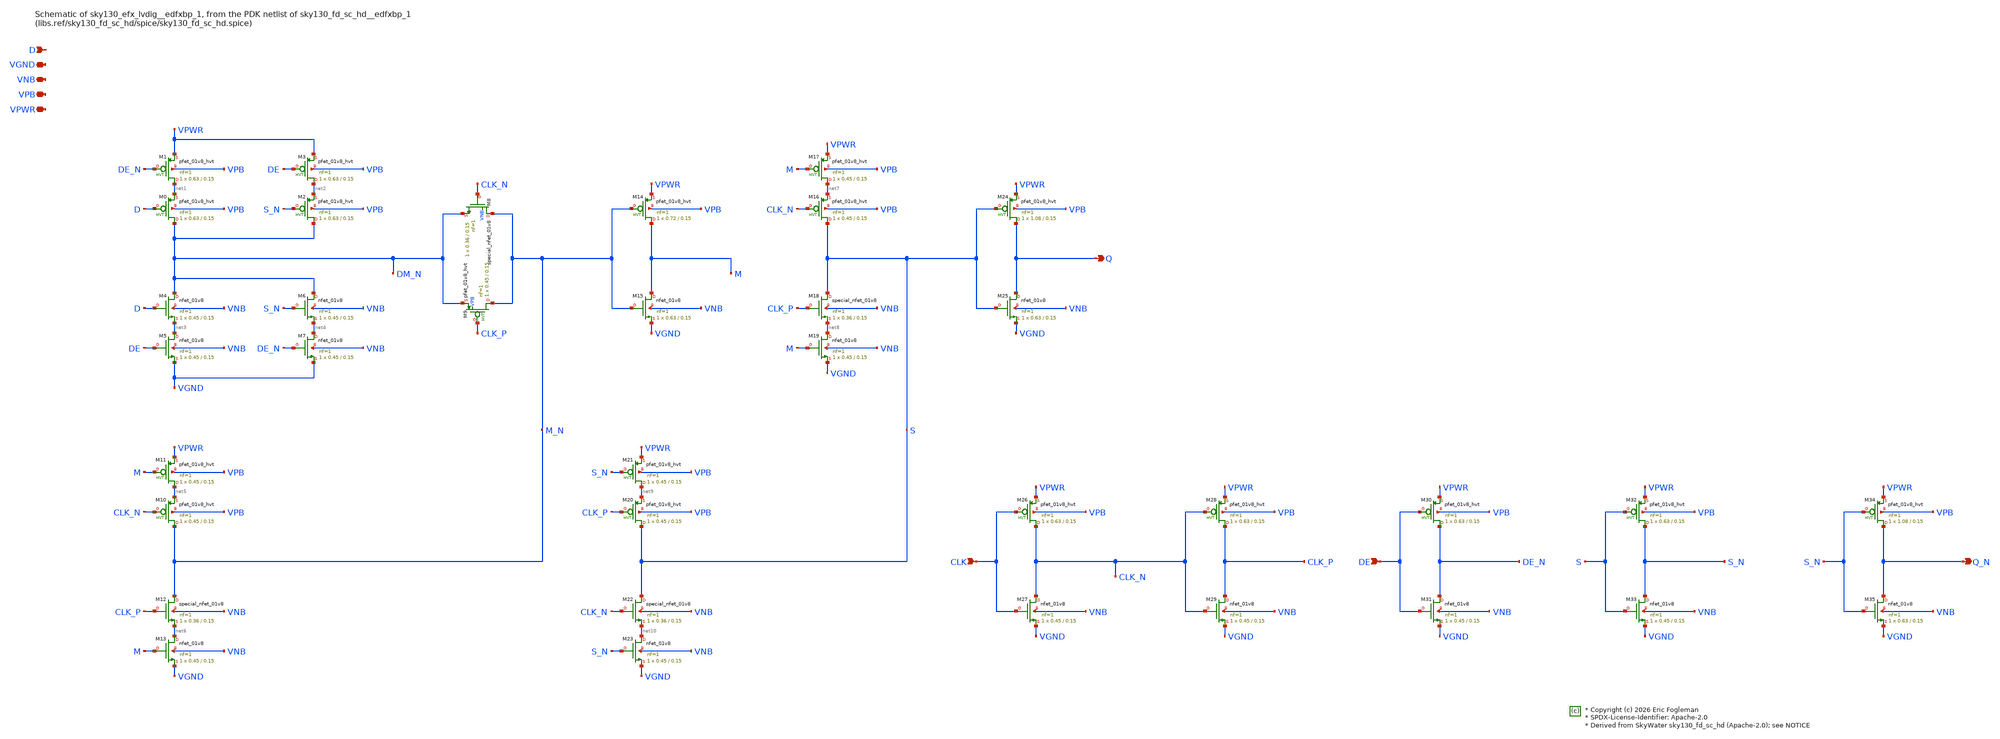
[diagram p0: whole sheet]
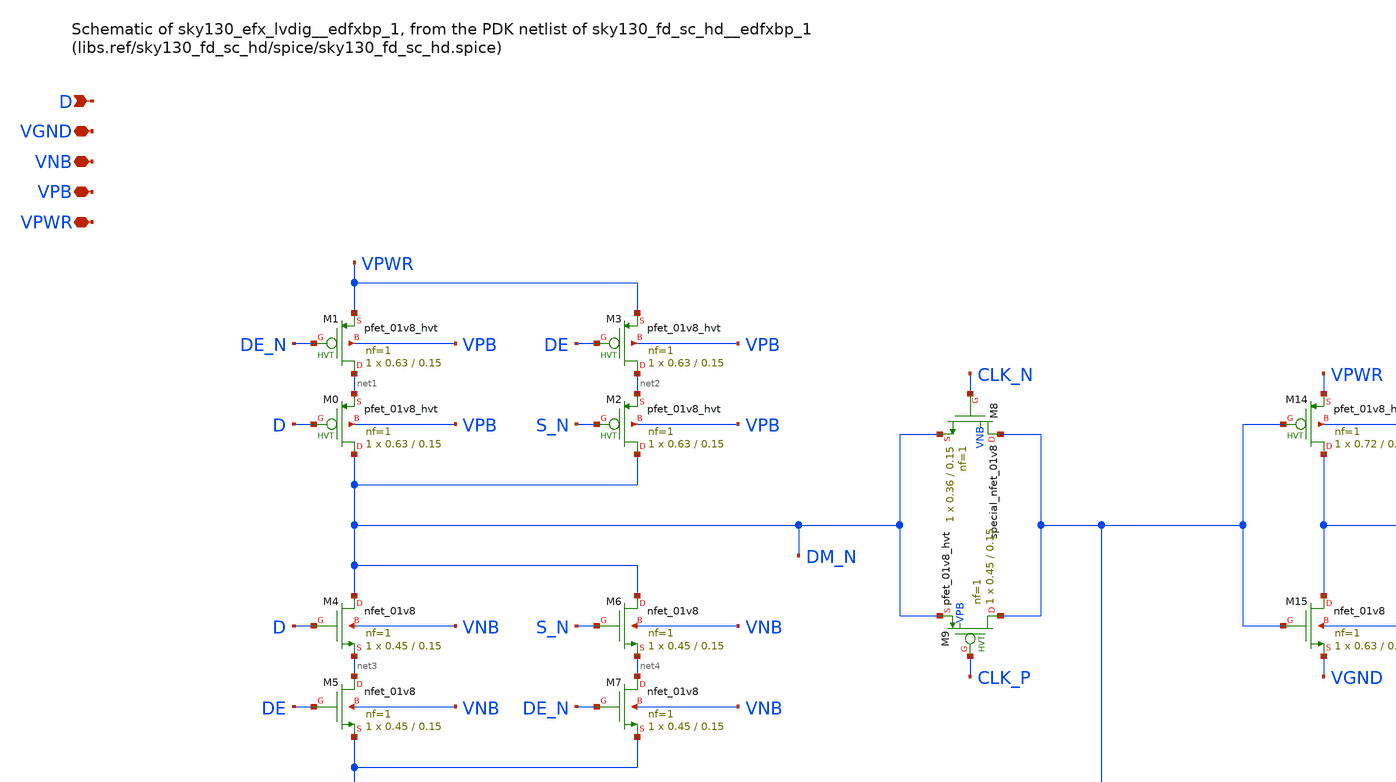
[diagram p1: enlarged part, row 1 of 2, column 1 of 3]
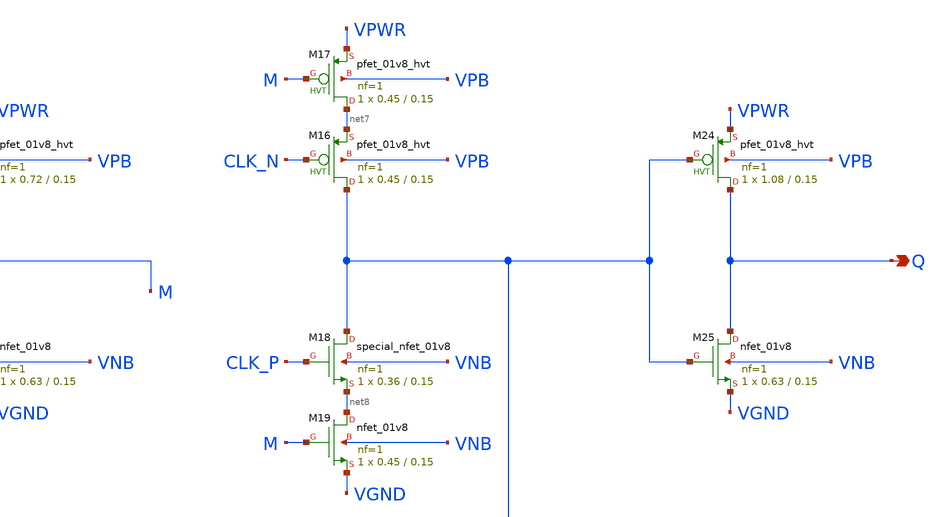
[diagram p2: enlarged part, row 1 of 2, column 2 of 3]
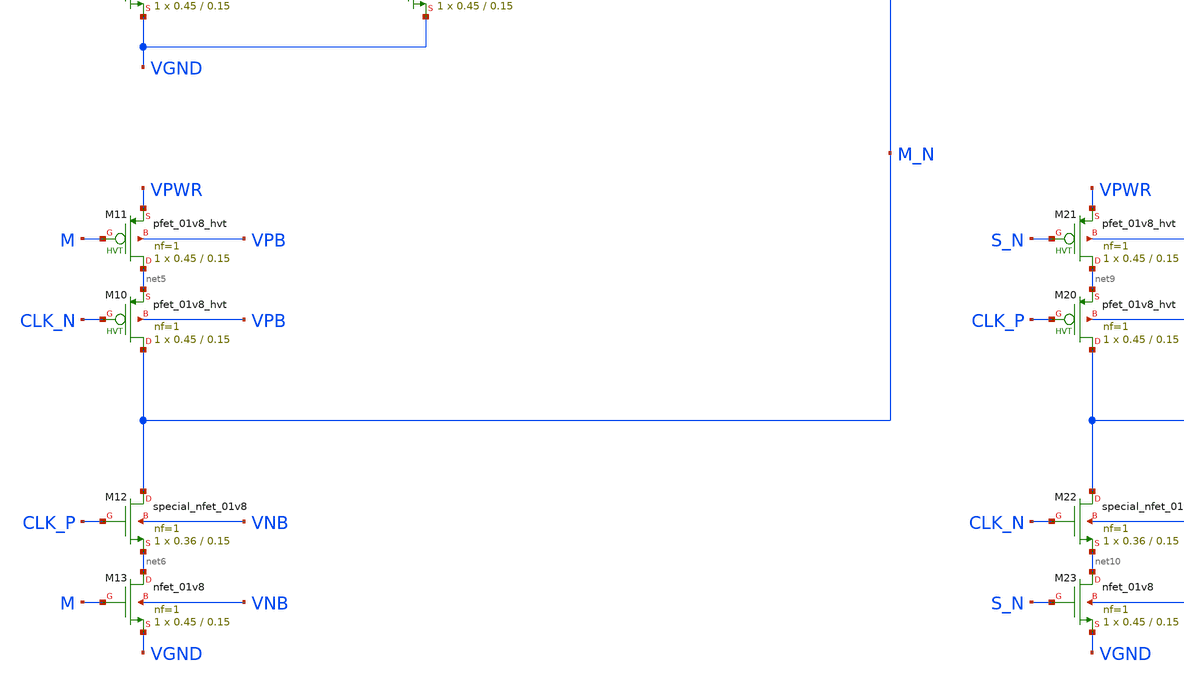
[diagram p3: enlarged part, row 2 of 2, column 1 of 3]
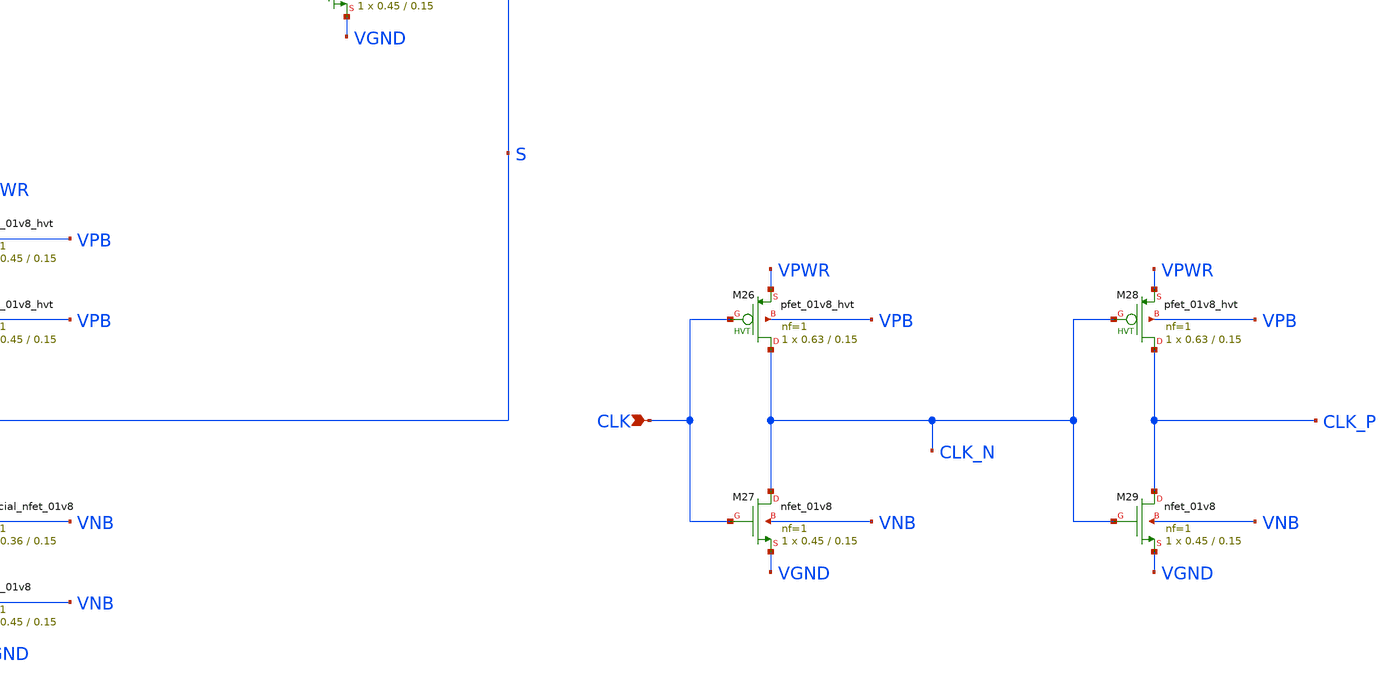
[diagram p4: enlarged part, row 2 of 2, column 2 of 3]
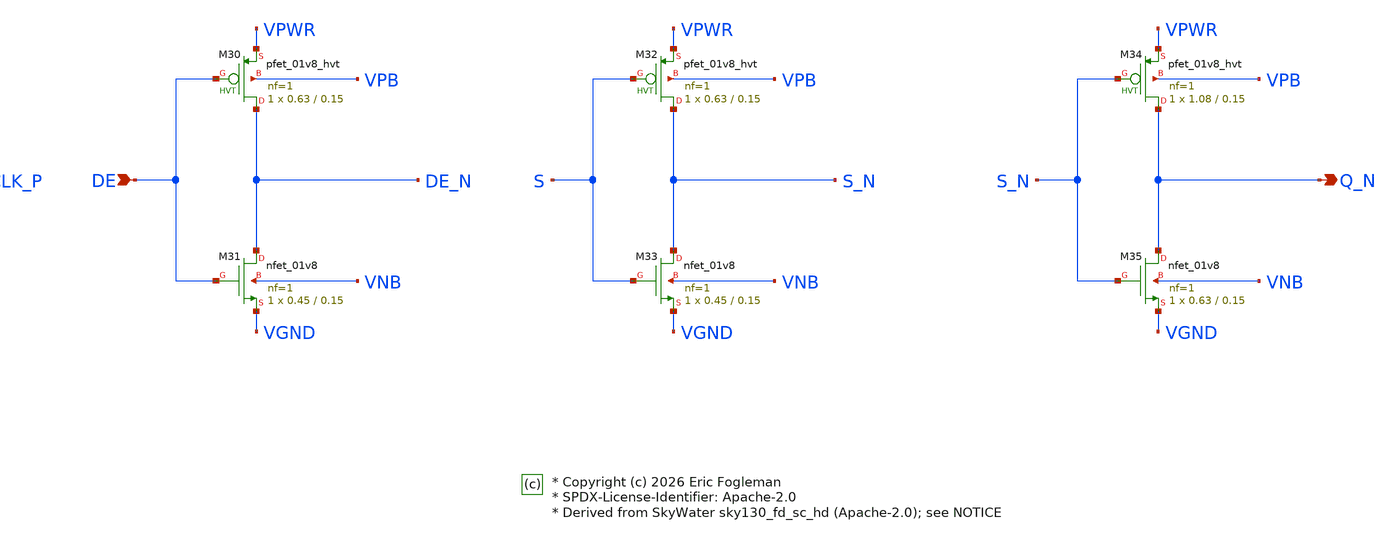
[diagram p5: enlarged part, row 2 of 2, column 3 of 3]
** sch_path: xschem/sky130_efx_lvdig__edfxbp_1.sch

* Copyright (c) 2026 Eric Fogleman
* SPDX-License-Identifier: Apache-2.0
* Derived from SkyWater sky130_fd_sc_hd (Apache-2.0); see NOTICE

**.subckt sky130_efx_lvdig__edfxbp_1 Q CLK DE Q_N D VGND VNB VPB VPWR
*.opin Q
*.ipin CLK
*.ipin DE
*.opin Q_N
*.ipin D
*.iopin VGND
*.iopin VNB
*.iopin VPB
*.iopin VPWR
XM0 DM_N D net1 VPB sky130_fd_pr__pfet_01v8_hvt L=0.15 W=0.63 nf=1 ad='int((1 + 1)/2) * 0.63 / 1 * 0.29'
+ as='int((1 + 2)/2) * 0.63 / 1 * 0.29' pd='2*int((1 + 1)/2) * (0.63 / 1 + 0.29)' ps='2*int((1 + 2)/2) * (0.63 / 1 + 0.29)'
+ nrd='0.29 / 0.63 ' nrs='0.29 / 0.63 ' sa=0 sb=0 sd=0 mult=1 m=1
XM1 net1 DE_N VPWR VPB sky130_fd_pr__pfet_01v8_hvt L=0.15 W=0.63 nf=1 ad='int((1 + 1)/2) * 0.63 / 1 * 0.29'
+ as='int((1 + 2)/2) * 0.63 / 1 * 0.29' pd='2*int((1 + 1)/2) * (0.63 / 1 + 0.29)' ps='2*int((1 + 2)/2) * (0.63 / 1 + 0.29)'
+ nrd='0.29 / 0.63 ' nrs='0.29 / 0.63 ' sa=0 sb=0 sd=0 mult=1 m=1
XM2 DM_N S_N net2 VPB sky130_fd_pr__pfet_01v8_hvt L=0.15 W=0.63 nf=1 ad='int((1 + 1)/2) * 0.63 / 1 * 0.29'
+ as='int((1 + 2)/2) * 0.63 / 1 * 0.29' pd='2*int((1 + 1)/2) * (0.63 / 1 + 0.29)' ps='2*int((1 + 2)/2) * (0.63 / 1 + 0.29)'
+ nrd='0.29 / 0.63 ' nrs='0.29 / 0.63 ' sa=0 sb=0 sd=0 mult=1 m=1
XM3 net2 DE VPWR VPB sky130_fd_pr__pfet_01v8_hvt L=0.15 W=0.63 nf=1 ad='int((1 + 1)/2) * 0.63 / 1 * 0.29'
+ as='int((1 + 2)/2) * 0.63 / 1 * 0.29' pd='2*int((1 + 1)/2) * (0.63 / 1 + 0.29)' ps='2*int((1 + 2)/2) * (0.63 / 1 + 0.29)'
+ nrd='0.29 / 0.63 ' nrs='0.29 / 0.63 ' sa=0 sb=0 sd=0 mult=1 m=1
XM4 DM_N D net3 VNB sky130_fd_pr__nfet_01v8 L=0.15 W=0.45 nf=1 ad='int((1 + 1)/2) * 0.45 / 1 * 0.29'
+ as='int((1 + 2)/2) * 0.45 / 1 * 0.29' pd='2*int((1 + 1)/2) * (0.45 / 1 + 0.29)' ps='2*int((1 + 2)/2) * (0.45 / 1 + 0.29)'
+ nrd='0.29 / 0.45 ' nrs='0.29 / 0.45 ' sa=0 sb=0 sd=0 mult=1 m=1
XM5 net3 DE VGND VNB sky130_fd_pr__nfet_01v8 L=0.15 W=0.45 nf=1 ad='int((1 + 1)/2) * 0.45 / 1 * 0.29'
+ as='int((1 + 2)/2) * 0.45 / 1 * 0.29' pd='2*int((1 + 1)/2) * (0.45 / 1 + 0.29)' ps='2*int((1 + 2)/2) * (0.45 / 1 + 0.29)'
+ nrd='0.29 / 0.45 ' nrs='0.29 / 0.45 ' sa=0 sb=0 sd=0 mult=1 m=1
XM6 DM_N S_N net4 VNB sky130_fd_pr__nfet_01v8 L=0.15 W=0.45 nf=1 ad='int((1 + 1)/2) * 0.45 / 1 * 0.29'
+ as='int((1 + 2)/2) * 0.45 / 1 * 0.29' pd='2*int((1 + 1)/2) * (0.45 / 1 + 0.29)' ps='2*int((1 + 2)/2) * (0.45 / 1 + 0.29)'
+ nrd='0.29 / 0.45 ' nrs='0.29 / 0.45 ' sa=0 sb=0 sd=0 mult=1 m=1
XM7 net4 DE_N VGND VNB sky130_fd_pr__nfet_01v8 L=0.15 W=0.45 nf=1 ad='int((1 + 1)/2) * 0.45 / 1 * 0.29'
+ as='int((1 + 2)/2) * 0.45 / 1 * 0.29' pd='2*int((1 + 1)/2) * (0.45 / 1 + 0.29)' ps='2*int((1 + 2)/2) * (0.45 / 1 + 0.29)'
+ nrd='0.29 / 0.45 ' nrs='0.29 / 0.45 ' sa=0 sb=0 sd=0 mult=1 m=1
XM8 M_N CLK_N DM_N VNB sky130_fd_pr__special_nfet_01v8 L=0.15 W=0.36 nf=1 ad='int((nf+1)/2) * W/nf * 0.29'
+ as='int((nf+2)/2) * W/nf * 0.29' pd='2*int((nf+1)/2) * (W/nf + 0.29)' ps='2*int((nf+2)/2) * (W/nf + 0.29)'
+ nrd='0.29 / W' nrs='0.29 / W' sa=0 sb=0 sd=0 mult=1 m=1
XM9 M_N CLK_P DM_N VPB sky130_fd_pr__pfet_01v8_hvt L=0.15 W=0.45 nf=1 ad='int((1 + 1)/2) * 0.45 / 1 * 0.29'
+ as='int((1 + 2)/2) * 0.45 / 1 * 0.29' pd='2*int((1 + 1)/2) * (0.45 / 1 + 0.29)' ps='2*int((1 + 2)/2) * (0.45 / 1 + 0.29)'
+ nrd='0.29 / 0.45 ' nrs='0.29 / 0.45 ' sa=0 sb=0 sd=0 mult=1 m=1
XM10 M_N CLK_N net5 VPB sky130_fd_pr__pfet_01v8_hvt L=0.15 W=0.45 nf=1 ad='int((1 + 1)/2) * 0.45 / 1 * 0.29'
+ as='int((1 + 2)/2) * 0.45 / 1 * 0.29' pd='2*int((1 + 1)/2) * (0.45 / 1 + 0.29)' ps='2*int((1 + 2)/2) * (0.45 / 1 + 0.29)'
+ nrd='0.29 / 0.45 ' nrs='0.29 / 0.45 ' sa=0 sb=0 sd=0 mult=1 m=1
XM11 net5 M VPWR VPB sky130_fd_pr__pfet_01v8_hvt L=0.15 W=0.45 nf=1 ad='int((1 + 1)/2) * 0.45 / 1 * 0.29'
+ as='int((1 + 2)/2) * 0.45 / 1 * 0.29' pd='2*int((1 + 1)/2) * (0.45 / 1 + 0.29)' ps='2*int((1 + 2)/2) * (0.45 / 1 + 0.29)'
+ nrd='0.29 / 0.45 ' nrs='0.29 / 0.45 ' sa=0 sb=0 sd=0 mult=1 m=1
XM12 M_N CLK_P net6 VNB sky130_fd_pr__special_nfet_01v8 L=0.15 W=0.36 nf=1 ad='int((1 + 1)/2) * 0.36 / 1 * 0.29'
+ as='int((1 + 2)/2) * 0.36 / 1 * 0.29' pd='2*int((1 + 1)/2) * (0.36 / 1 + 0.29)' ps='2*int((1 + 2)/2) * (0.36 / 1 + 0.29)'
+ nrd='0.29 / 0.36 ' nrs='0.29 / 0.36 ' sa=0 sb=0 sd=0 mult=1 m=1
XM13 net6 M VGND VNB sky130_fd_pr__nfet_01v8 L=0.15 W=0.45 nf=1 ad='int((1 + 1)/2) * 0.45 / 1 * 0.29'
+ as='int((1 + 2)/2) * 0.45 / 1 * 0.29' pd='2*int((1 + 1)/2) * (0.45 / 1 + 0.29)' ps='2*int((1 + 2)/2) * (0.45 / 1 + 0.29)'
+ nrd='0.29 / 0.45 ' nrs='0.29 / 0.45 ' sa=0 sb=0 sd=0 mult=1 m=1
XM14 M M_N VPWR VPB sky130_fd_pr__pfet_01v8_hvt L=0.15 W=0.72 nf=1 ad='int((1 + 1)/2) * 0.72 / 1 * 0.29'
+ as='int((1 + 2)/2) * 0.72 / 1 * 0.29' pd='2*int((1 + 1)/2) * (0.72 / 1 + 0.29)' ps='2*int((1 + 2)/2) * (0.72 / 1 + 0.29)'
+ nrd='0.29 / 0.72 ' nrs='0.29 / 0.72 ' sa=0 sb=0 sd=0 mult=1 m=1
XM15 M M_N VGND VNB sky130_fd_pr__nfet_01v8 L=0.15 W=0.63 nf=1 ad='int((1 + 1)/2) * 0.63 / 1 * 0.29'
+ as='int((1 + 2)/2) * 0.63 / 1 * 0.29' pd='2*int((1 + 1)/2) * (0.63 / 1 + 0.29)' ps='2*int((1 + 2)/2) * (0.63 / 1 + 0.29)'
+ nrd='0.29 / 0.63 ' nrs='0.29 / 0.63 ' sa=0 sb=0 sd=0 mult=1 m=1
XM16 S CLK_N net7 VPB sky130_fd_pr__pfet_01v8_hvt L=0.15 W=0.45 nf=1 ad='int((1 + 1)/2) * 0.45 / 1 * 0.29'
+ as='int((1 + 2)/2) * 0.45 / 1 * 0.29' pd='2*int((1 + 1)/2) * (0.45 / 1 + 0.29)' ps='2*int((1 + 2)/2) * (0.45 / 1 + 0.29)'
+ nrd='0.29 / 0.45 ' nrs='0.29 / 0.45 ' sa=0 sb=0 sd=0 mult=1 m=1
XM17 net7 M VPWR VPB sky130_fd_pr__pfet_01v8_hvt L=0.15 W=0.45 nf=1 ad='int((1 + 1)/2) * 0.45 / 1 * 0.29'
+ as='int((1 + 2)/2) * 0.45 / 1 * 0.29' pd='2*int((1 + 1)/2) * (0.45 / 1 + 0.29)' ps='2*int((1 + 2)/2) * (0.45 / 1 + 0.29)'
+ nrd='0.29 / 0.45 ' nrs='0.29 / 0.45 ' sa=0 sb=0 sd=0 mult=1 m=1
XM18 S CLK_P net8 VNB sky130_fd_pr__special_nfet_01v8 L=0.15 W=0.36 nf=1 ad='int((1 + 1)/2) * 0.36 / 1 * 0.29'
+ as='int((1 + 2)/2) * 0.36 / 1 * 0.29' pd='2*int((1 + 1)/2) * (0.36 / 1 + 0.29)' ps='2*int((1 + 2)/2) * (0.36 / 1 + 0.29)'
+ nrd='0.29 / 0.36 ' nrs='0.29 / 0.36 ' sa=0 sb=0 sd=0 mult=1 m=1
XM19 net8 M VGND VNB sky130_fd_pr__nfet_01v8 L=0.15 W=0.45 nf=1 ad='int((1 + 1)/2) * 0.45 / 1 * 0.29'
+ as='int((1 + 2)/2) * 0.45 / 1 * 0.29' pd='2*int((1 + 1)/2) * (0.45 / 1 + 0.29)' ps='2*int((1 + 2)/2) * (0.45 / 1 + 0.29)'
+ nrd='0.29 / 0.45 ' nrs='0.29 / 0.45 ' sa=0 sb=0 sd=0 mult=1 m=1
XM20 S CLK_P net9 VPB sky130_fd_pr__pfet_01v8_hvt L=0.15 W=0.45 nf=1 ad='int((1 + 1)/2) * 0.45 / 1 * 0.29'
+ as='int((1 + 2)/2) * 0.45 / 1 * 0.29' pd='2*int((1 + 1)/2) * (0.45 / 1 + 0.29)' ps='2*int((1 + 2)/2) * (0.45 / 1 + 0.29)'
+ nrd='0.29 / 0.45 ' nrs='0.29 / 0.45 ' sa=0 sb=0 sd=0 mult=1 m=1
XM21 net9 S_N VPWR VPB sky130_fd_pr__pfet_01v8_hvt L=0.15 W=0.45 nf=1 ad='int((1 + 1)/2) * 0.45 / 1 * 0.29'
+ as='int((1 + 2)/2) * 0.45 / 1 * 0.29' pd='2*int((1 + 1)/2) * (0.45 / 1 + 0.29)' ps='2*int((1 + 2)/2) * (0.45 / 1 + 0.29)'
+ nrd='0.29 / 0.45 ' nrs='0.29 / 0.45 ' sa=0 sb=0 sd=0 mult=1 m=1
XM22 S CLK_N net10 VNB sky130_fd_pr__special_nfet_01v8 L=0.15 W=0.36 nf=1 ad='int((1 + 1)/2) * 0.36 / 1 * 0.29'
+ as='int((1 + 2)/2) * 0.36 / 1 * 0.29' pd='2*int((1 + 1)/2) * (0.36 / 1 + 0.29)' ps='2*int((1 + 2)/2) * (0.36 / 1 + 0.29)'
+ nrd='0.29 / 0.36 ' nrs='0.29 / 0.36 ' sa=0 sb=0 sd=0 mult=1 m=1
XM23 net10 S_N VGND VNB sky130_fd_pr__nfet_01v8 L=0.15 W=0.45 nf=1 ad='int((1 + 1)/2) * 0.45 / 1 * 0.29'
+ as='int((1 + 2)/2) * 0.45 / 1 * 0.29' pd='2*int((1 + 1)/2) * (0.45 / 1 + 0.29)' ps='2*int((1 + 2)/2) * (0.45 / 1 + 0.29)'
+ nrd='0.29 / 0.45 ' nrs='0.29 / 0.45 ' sa=0 sb=0 sd=0 mult=1 m=1
XM24 Q S VPWR VPB sky130_fd_pr__pfet_01v8_hvt L=0.15 W=1.08 nf=1 ad='int((1 + 1)/2) * 1.08 / 1 * 0.29'
+ as='int((1 + 2)/2) * 1.08 / 1 * 0.29' pd='2*int((1 + 1)/2) * (1.08 / 1 + 0.29)' ps='2*int((1 + 2)/2) * (1.08 / 1 + 0.29)'
+ nrd='0.29 / 1.08 ' nrs='0.29 / 1.08 ' sa=0 sb=0 sd=0 mult=1 m=1
XM25 Q S VGND VNB sky130_fd_pr__nfet_01v8 L=0.15 W=0.63 nf=1 ad='int((1 + 1)/2) * 0.63 / 1 * 0.29' as='int((1 + 2)/2) * 0.63 / 1 * 0.29'
+ pd='2*int((1 + 1)/2) * (0.63 / 1 + 0.29)' ps='2*int((1 + 2)/2) * (0.63 / 1 + 0.29)' nrd='0.29 / 0.63 '
+ nrs='0.29 / 0.63 ' sa=0 sb=0 sd=0 mult=1 m=1
XM26 CLK_N CLK VPWR VPB sky130_fd_pr__pfet_01v8_hvt L=0.15 W=0.63 nf=1 ad='int((1 + 1)/2) * 0.63 / 1 * 0.29'
+ as='int((1 + 2)/2) * 0.63 / 1 * 0.29' pd='2*int((1 + 1)/2) * (0.63 / 1 + 0.29)' ps='2*int((1 + 2)/2) * (0.63 / 1 + 0.29)'
+ nrd='0.29 / 0.63 ' nrs='0.29 / 0.63 ' sa=0 sb=0 sd=0 mult=1 m=1
XM27 CLK_N CLK VGND VNB sky130_fd_pr__nfet_01v8 L=0.15 W=0.45 nf=1 ad='int((1 + 1)/2) * 0.45 / 1 * 0.29'
+ as='int((1 + 2)/2) * 0.45 / 1 * 0.29' pd='2*int((1 + 1)/2) * (0.45 / 1 + 0.29)' ps='2*int((1 + 2)/2) * (0.45 / 1 + 0.29)'
+ nrd='0.29 / 0.45 ' nrs='0.29 / 0.45 ' sa=0 sb=0 sd=0 mult=1 m=1
XM28 CLK_P CLK_N VPWR VPB sky130_fd_pr__pfet_01v8_hvt L=0.15 W=0.63 nf=1 ad='int((1 + 1)/2) * 0.63 / 1 * 0.29'
+ as='int((1 + 2)/2) * 0.63 / 1 * 0.29' pd='2*int((1 + 1)/2) * (0.63 / 1 + 0.29)' ps='2*int((1 + 2)/2) * (0.63 / 1 + 0.29)'
+ nrd='0.29 / 0.63 ' nrs='0.29 / 0.63 ' sa=0 sb=0 sd=0 mult=1 m=1
XM29 CLK_P CLK_N VGND VNB sky130_fd_pr__nfet_01v8 L=0.15 W=0.45 nf=1 ad='int((1 + 1)/2) * 0.45 / 1 * 0.29'
+ as='int((1 + 2)/2) * 0.45 / 1 * 0.29' pd='2*int((1 + 1)/2) * (0.45 / 1 + 0.29)' ps='2*int((1 + 2)/2) * (0.45 / 1 + 0.29)'
+ nrd='0.29 / 0.45 ' nrs='0.29 / 0.45 ' sa=0 sb=0 sd=0 mult=1 m=1
XM30 DE_N DE VPWR VPB sky130_fd_pr__pfet_01v8_hvt L=0.15 W=0.63 nf=1 ad='int((1 + 1)/2) * 0.63 / 1 * 0.29'
+ as='int((1 + 2)/2) * 0.63 / 1 * 0.29' pd='2*int((1 + 1)/2) * (0.63 / 1 + 0.29)' ps='2*int((1 + 2)/2) * (0.63 / 1 + 0.29)'
+ nrd='0.29 / 0.63 ' nrs='0.29 / 0.63 ' sa=0 sb=0 sd=0 mult=1 m=1
XM31 DE_N DE VGND VNB sky130_fd_pr__nfet_01v8 L=0.15 W=0.45 nf=1 ad='int((1 + 1)/2) * 0.45 / 1 * 0.29'
+ as='int((1 + 2)/2) * 0.45 / 1 * 0.29' pd='2*int((1 + 1)/2) * (0.45 / 1 + 0.29)' ps='2*int((1 + 2)/2) * (0.45 / 1 + 0.29)'
+ nrd='0.29 / 0.45 ' nrs='0.29 / 0.45 ' sa=0 sb=0 sd=0 mult=1 m=1
XM32 S_N S VPWR VPB sky130_fd_pr__pfet_01v8_hvt L=0.15 W=0.63 nf=1 ad='int((1 + 1)/2) * 0.63 / 1 * 0.29'
+ as='int((1 + 2)/2) * 0.63 / 1 * 0.29' pd='2*int((1 + 1)/2) * (0.63 / 1 + 0.29)' ps='2*int((1 + 2)/2) * (0.63 / 1 + 0.29)'
+ nrd='0.29 / 0.63 ' nrs='0.29 / 0.63 ' sa=0 sb=0 sd=0 mult=1 m=1
XM33 S_N S VGND VNB sky130_fd_pr__nfet_01v8 L=0.15 W=0.45 nf=1 ad='int((1 + 1)/2) * 0.45 / 1 * 0.29'
+ as='int((1 + 2)/2) * 0.45 / 1 * 0.29' pd='2*int((1 + 1)/2) * (0.45 / 1 + 0.29)' ps='2*int((1 + 2)/2) * (0.45 / 1 + 0.29)'
+ nrd='0.29 / 0.45 ' nrs='0.29 / 0.45 ' sa=0 sb=0 sd=0 mult=1 m=1
XM34 Q_N S_N VPWR VPB sky130_fd_pr__pfet_01v8_hvt L=0.15 W=1.08 nf=1 ad='int((1 + 1)/2) * 1.08 / 1 * 0.29'
+ as='int((1 + 2)/2) * 1.08 / 1 * 0.29' pd='2*int((1 + 1)/2) * (1.08 / 1 + 0.29)' ps='2*int((1 + 2)/2) * (1.08 / 1 + 0.29)'
+ nrd='0.29 / 1.08 ' nrs='0.29 / 1.08 ' sa=0 sb=0 sd=0 mult=1 m=1
XM35 Q_N S_N VGND VNB sky130_fd_pr__nfet_01v8 L=0.15 W=0.63 nf=1 ad='int((1 + 1)/2) * 0.63 / 1 * 0.29'
+ as='int((1 + 2)/2) * 0.63 / 1 * 0.29' pd='2*int((1 + 1)/2) * (0.63 / 1 + 0.29)' ps='2*int((1 + 2)/2) * (0.63 / 1 + 0.29)'
+ nrd='0.29 / 0.63 ' nrs='0.29 / 0.63 ' sa=0 sb=0 sd=0 mult=1 m=1
**.ends
.end
